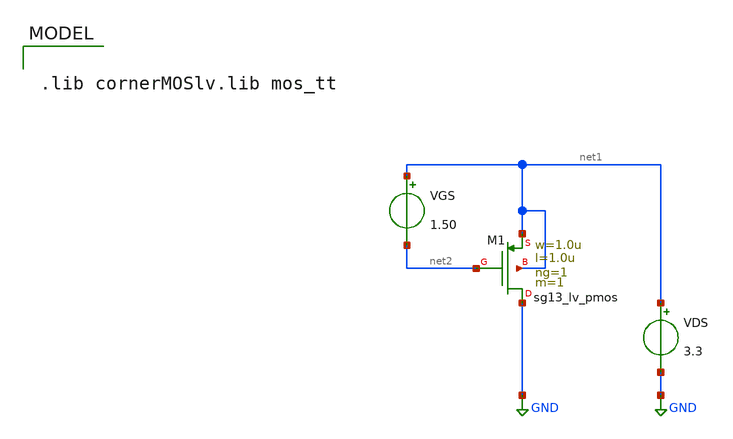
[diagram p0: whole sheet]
** sch_path: gmid/lv_pmos.sch
**.subckt lv_pmos
VGS net1 net2 1.50
VDS net1 GND 3.3
XM1 GND net2 net1 net1 sg13_lv_pmos w=1.0u l=1.0u ng=1 m=1 mm_ok=1
**** begin user architecture code

.lib cornerMOSlv.lib mos_tt



.option savecurrents
.save all @n.xm1.nsg13_lv_pmos[ids] @n.xm1.nsg13_lv_pmos[l] @n.xm1.nsg13_lv_pmos[gm] @n.xm1.nsg13_lv_pmos[cgg] @n.xm1.nsg13_lv_pmos[gds] @n.xm1.nsg13_lv_pmos[vgs] @n.xm1.nsg13_lv_pmos[vds]
.control

.param L=1e-6

set wr_singlescale
set wr_vecnames
set appendwrite

let start_L = 1e-6
let stop_L = 50e-6
let delta_L = 1e-6

let start_VDS = 0
let stop_VDS = 3.4
let delta_VDS = 0.1

let actual_L = start_L

while actual_L le stop_L
	alter @n.xm1.nsg13_lv_pmos[l] = actual_L
	let actual_VDS = start_VDS
	while actual_VDS le stop_VDS
		alter VDS actual_VDS
		dc VGS 0 3.3 0.01
		wrdata lv_pmos.txt @n.xm1.nsg13_lv_pmos[vgs] @n.xm1.nsg13_lv_pmos[vds] @n.xm1.nsg13_lv_pmos[ids]
+ @n.xm1.nsg13_lv_pmos[l] @n.xm1.nsg13_lv_pmos[gm] @n.xm1.nsg13_lv_pmos[cgg] @n.xm1.nsg13_lv_pmos[gds]
		let actual_VDS = actual_VDS + delta_VDS
	end
	let actual_L = actual_L + delta_L
end

write lv_nmos.raw

.endc



**** end user architecture code
**.ends
.GLOBAL GND
.end
